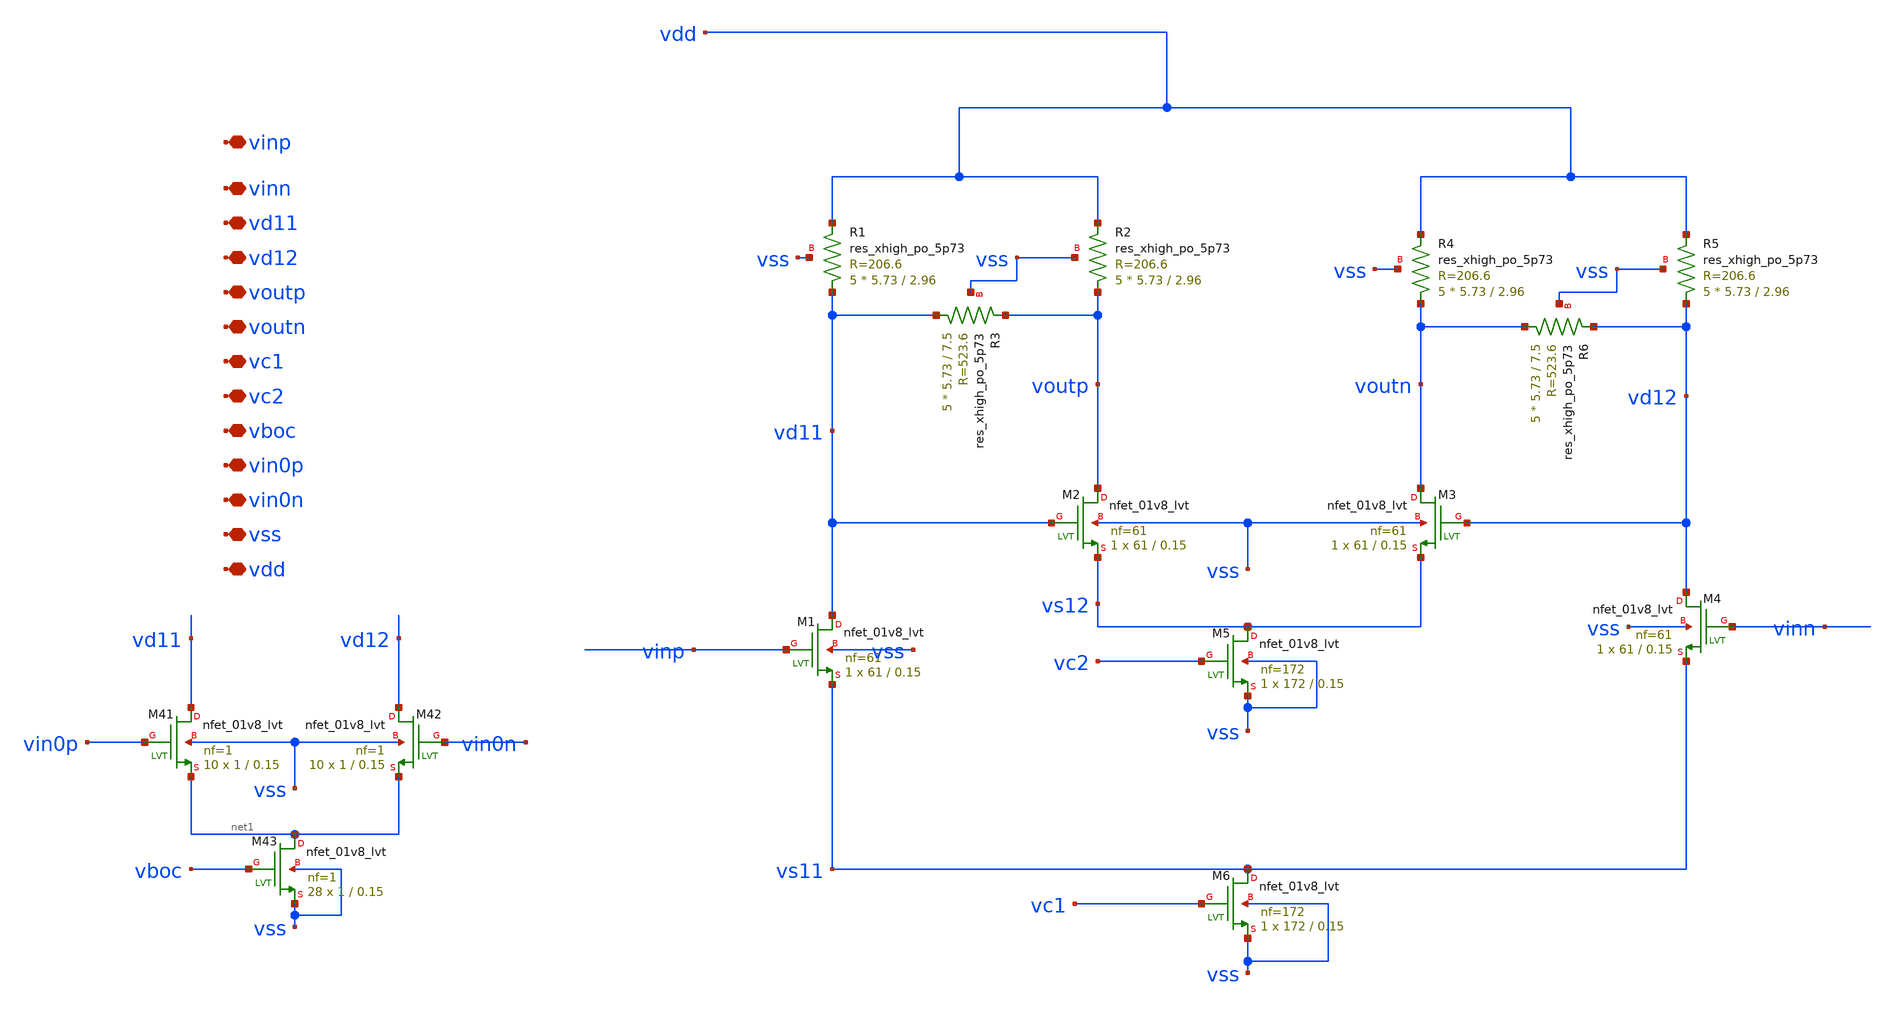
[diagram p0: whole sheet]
** sch_path: design/vga/1stage_lo.sch
**.subckt 1stage_lo vinp vinn vd11 vd12 voutp voutn vc1 vc2 vboc vin0p vin0n vss vdd
*.iopin vinp
*.iopin vinn
*.iopin vd11
*.iopin vd12
*.iopin voutp
*.iopin voutn
*.iopin vc1
*.iopin vc2
*.iopin vboc
*.iopin vin0p
*.iopin vin0n
*.iopin vss
*.iopin vdd
XR1 vd11 vdd vss sky130_fd_pr__res_xhigh_po_5p73 L=2.96 mult=5 m=5
XR2 voutp vdd vss sky130_fd_pr__res_xhigh_po_5p73 L=2.96 mult=5 m=5
XR3 vd11 voutp vss sky130_fd_pr__res_xhigh_po_5p73 L=7.5 mult=5 m=5
XR4 voutn vdd vss sky130_fd_pr__res_xhigh_po_5p73 L=2.96 mult=5 m=5
XR5 vd12 vdd vss sky130_fd_pr__res_xhigh_po_5p73 L=2.96 mult=5 m=5
XR6 voutn vd12 vss sky130_fd_pr__res_xhigh_po_5p73 L=7.5 mult=5 m=5
XM1 vd11 vinp vs11 vss sky130_fd_pr__nfet_01v8_lvt L=0.15 W=61 nf=61 ad='int((nf+1)/2) * W/nf * 0.29'
+ as='int((nf+2)/2) * W/nf * 0.29' pd='2*int((nf+1)/2) * (W/nf + 0.29)' ps='2*int((nf+2)/2) * (W/nf + 0.29)'
+ nrd='0.29 / W' nrs='0.29 / W' sa=0 sb=0 sd=0 mult=1 m=1
XM2 voutp vd11 vs12 vss sky130_fd_pr__nfet_01v8_lvt L=0.15 W=61 nf=61 ad='int((nf+1)/2) * W/nf * 0.29'
+ as='int((nf+2)/2) * W/nf * 0.29' pd='2*int((nf+1)/2) * (W/nf + 0.29)' ps='2*int((nf+2)/2) * (W/nf + 0.29)'
+ nrd='0.29 / W' nrs='0.29 / W' sa=0 sb=0 sd=0 mult=1 m=1
XM3 voutn vd12 vs12 vss sky130_fd_pr__nfet_01v8_lvt L=0.15 W=61 nf=61 ad='int((nf+1)/2) * W/nf * 0.29'
+ as='int((nf+2)/2) * W/nf * 0.29' pd='2*int((nf+1)/2) * (W/nf + 0.29)' ps='2*int((nf+2)/2) * (W/nf + 0.29)'
+ nrd='0.29 / W' nrs='0.29 / W' sa=0 sb=0 sd=0 mult=1 m=1
XM4 vd12 vinn vs11 vss sky130_fd_pr__nfet_01v8_lvt L=0.15 W=61 nf=61 ad='int((nf+1)/2) * W/nf * 0.29'
+ as='int((nf+2)/2) * W/nf * 0.29' pd='2*int((nf+1)/2) * (W/nf + 0.29)' ps='2*int((nf+2)/2) * (W/nf + 0.29)'
+ nrd='0.29 / W' nrs='0.29 / W' sa=0 sb=0 sd=0 mult=1 m=1
XM5 vs12 vc2 vss vss sky130_fd_pr__nfet_01v8_lvt L=0.15 W=172 nf=172 ad='int((nf+1)/2) * W/nf * 0.29'
+ as='int((nf+2)/2) * W/nf * 0.29' pd='2*int((nf+1)/2) * (W/nf + 0.29)' ps='2*int((nf+2)/2) * (W/nf + 0.29)'
+ nrd='0.29 / W' nrs='0.29 / W' sa=0 sb=0 sd=0 mult=1 m=1
XM6 vs11 vc1 vss vss sky130_fd_pr__nfet_01v8_lvt L=0.15 W=172 nf=172 ad='int((nf+1)/2) * W/nf * 0.29'
+ as='int((nf+2)/2) * W/nf * 0.29' pd='2*int((nf+1)/2) * (W/nf + 0.29)' ps='2*int((nf+2)/2) * (W/nf + 0.29)'
+ nrd='0.29 / W' nrs='0.29 / W' sa=0 sb=0 sd=0 mult=1 m=1
XM41 vd11 vin0p net1 vss sky130_fd_pr__nfet_01v8_lvt L=0.15 W=1 nf=1 ad='int((nf+1)/2) * W/nf * 0.29'
+ as='int((nf+2)/2) * W/nf * 0.29' pd='2*int((nf+1)/2) * (W/nf + 0.29)' ps='2*int((nf+2)/2) * (W/nf + 0.29)'
+ nrd='0.29 / W' nrs='0.29 / W' sa=0 sb=0 sd=0 mult=10 m=10
XM42 vd12 vin0n net1 vss sky130_fd_pr__nfet_01v8_lvt L=0.15 W=1 nf=1 ad='int((nf+1)/2) * W/nf * 0.29'
+ as='int((nf+2)/2) * W/nf * 0.29' pd='2*int((nf+1)/2) * (W/nf + 0.29)' ps='2*int((nf+2)/2) * (W/nf + 0.29)'
+ nrd='0.29 / W' nrs='0.29 / W' sa=0 sb=0 sd=0 mult=10 m=10
XM43 net1 vboc vss vss sky130_fd_pr__nfet_01v8_lvt L=0.15 W=1 nf=1 ad='int((nf+1)/2) * W/nf * 0.29' as='int((nf+2)/2) * W/nf * 0.29'
+ pd='2*int((nf+1)/2) * (W/nf + 0.29)' ps='2*int((nf+2)/2) * (W/nf + 0.29)' nrd='0.29 / W' nrs='0.29 / W'
+ sa=0 sb=0 sd=0 mult=28 m=28
**.ends
.end
